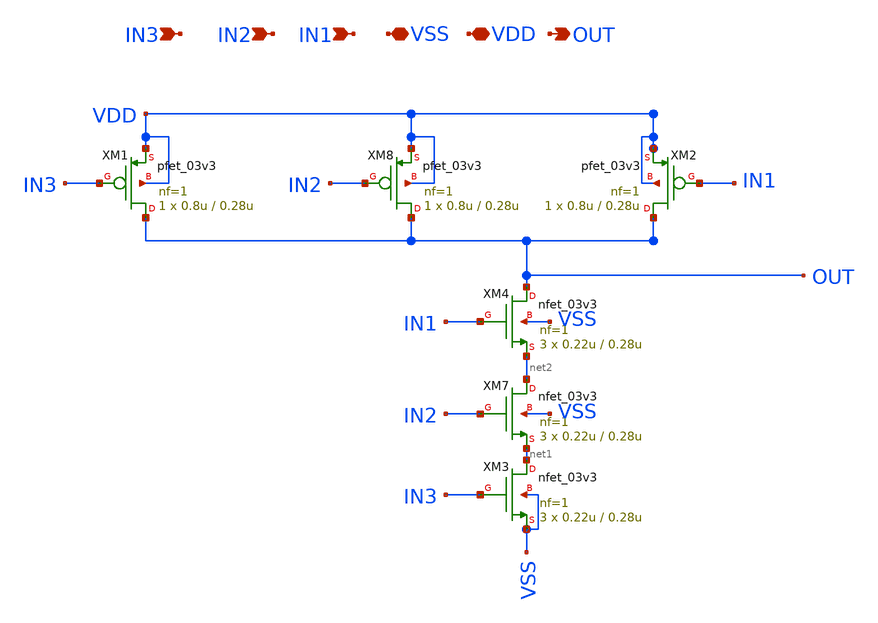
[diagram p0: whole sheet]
** sch_path: Clock_Generator_PAKISTAN_02/Schematics/nand3_ibr.sch
**.subckt nand3_ibr IN2 IN1 VSS VDD OUT IN3
*.ipin IN2
*.ipin IN1
*.iopin VSS
*.iopin VDD
*.opin OUT
*.ipin IN3
XM3 net1 IN3 VSS VSS nfet_03v3 L=0.28u W=0.22u nf=1 ad='int((nf+1)/2) * W/nf * 0.18u' as='int((nf+2)/2) * W/nf * 0.18u'
+ pd='2*int((nf+1)/2) * (W/nf + 0.18u)' ps='2*int((nf+2)/2) * (W/nf + 0.18u)' nrd='0.18u / W' nrs='0.18u / W'
+ sa=0 sb=0 sd=0 m=3
XM4 OUT IN1 net2 VSS nfet_03v3 L=0.28u W=0.22u nf=1 ad='int((nf+1)/2) * W/nf * 0.18u' as='int((nf+2)/2) * W/nf * 0.18u'
+ pd='2*int((nf+1)/2) * (W/nf + 0.18u)' ps='2*int((nf+2)/2) * (W/nf + 0.18u)' nrd='0.18u / W' nrs='0.18u / W'
+ sa=0 sb=0 sd=0 m=3
XM1 OUT IN3 VDD VDD pfet_03v3 L=0.28u W=0.8u nf=1 ad='int((nf+1)/2) * W/nf * 0.18u' as='int((nf+2)/2) * W/nf * 0.18u'
+ pd='2*int((nf+1)/2) * (W/nf + 0.18u)' ps='2*int((nf+2)/2) * (W/nf + 0.18u)' nrd='0.18u / W' nrs='0.18u / W'
+ sa=0 sb=0 sd=0 m=1
XM2 OUT IN1 VDD VDD pfet_03v3 L=0.28u W=0.8u nf=1 ad='int((nf+1)/2) * W/nf * 0.18u' as='int((nf+2)/2) * W/nf * 0.18u'
+ pd='2*int((nf+1)/2) * (W/nf + 0.18u)' ps='2*int((nf+2)/2) * (W/nf + 0.18u)' nrd='0.18u / W' nrs='0.18u / W'
+ sa=0 sb=0 sd=0 m=1
XM7 net2 IN2 net1 VSS nfet_03v3 L=0.28u W=0.22u nf=1 ad='int((nf+1)/2) * W/nf * 0.18u' as='int((nf+2)/2) * W/nf * 0.18u'
+ pd='2*int((nf+1)/2) * (W/nf + 0.18u)' ps='2*int((nf+2)/2) * (W/nf + 0.18u)' nrd='0.18u / W' nrs='0.18u / W'
+ sa=0 sb=0 sd=0 m=3
XM8 OUT IN2 VDD VDD pfet_03v3 L=0.28u W=0.8u nf=1 ad='int((nf+1)/2) * W/nf * 0.18u' as='int((nf+2)/2) * W/nf * 0.18u'
+ pd='2*int((nf+1)/2) * (W/nf + 0.18u)' ps='2*int((nf+2)/2) * (W/nf + 0.18u)' nrd='0.18u / W' nrs='0.18u / W'
+ sa=0 sb=0 sd=0 m=1
**.ends
.end
